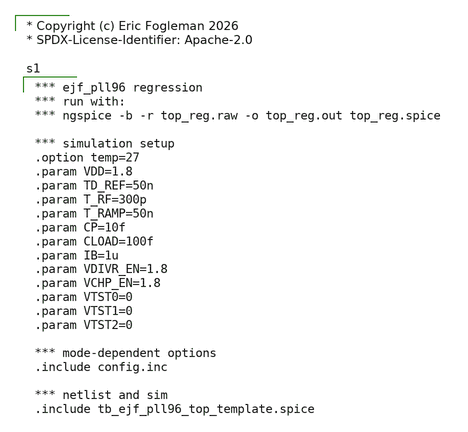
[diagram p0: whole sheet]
** sch_path: xschem/top_reg.sch

* Copyright (c) Eric Fogleman 2026
* SPDX-License-Identifier: Apache-2.0

**.subckt top_reg
**** begin user architecture code

*** ejf_pll96 regression
*** run with:
*** ngspice -b -r top_reg.raw -o top_reg.out top_reg.spice

*** simulation setup
.option temp=27
.param VDD=1.8
.param TD_REF=50n
.param T_RF=300p
.param T_RAMP=50n
.param CP=10f
.param CLOAD=100f
.param IB=1u
.param VDIVR_EN=1.8
.param VCHP_EN=1.8
.param VTST0=0
.param VTST1=0
.param VTST2=0

*** mode-dependent options
.include config.inc

*** netlist and sim
.include tb_ejf_pll96_top_template.spice


**** end user architecture code
**.ends
.end
